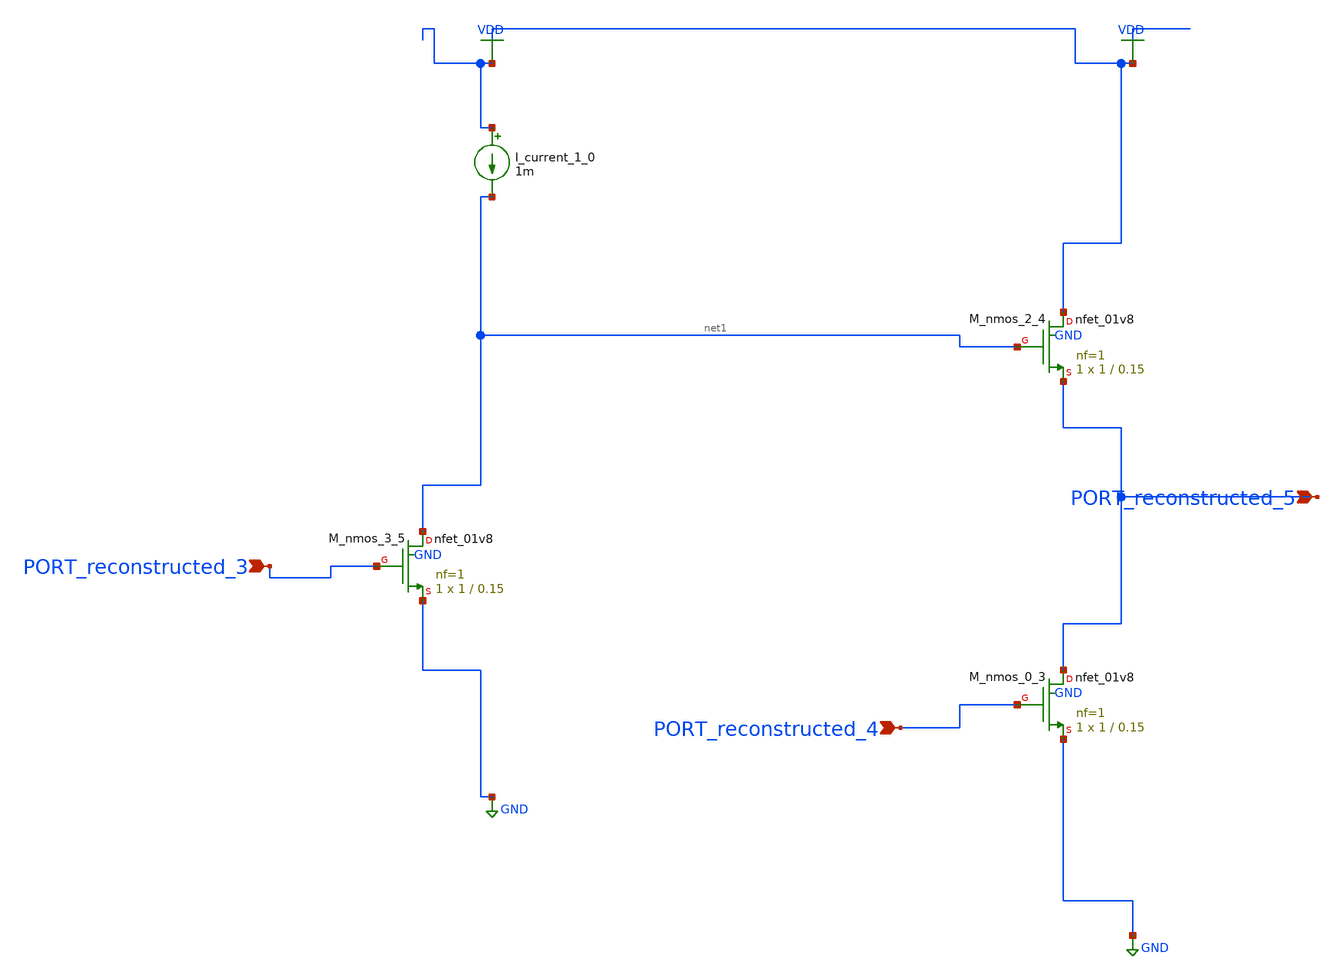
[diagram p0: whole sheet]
** sch_path: schematics/AMSNet/107.sch
**.subckt 107 PORT_reconstructed_4 PORT_reconstructed_3 PORT_reconstructed_5
*.ipin PORT_reconstructed_4
*.ipin PORT_reconstructed_3
*.ipin PORT_reconstructed_5
I_current_1_0 VDD net1 1m
XM_nmos_0_3 PORT_reconstructed_5 PORT_reconstructed_4 GND GND sky130_fd_pr__nfet_01v8 L=0.15 W=1 nf=1
+ ad='int((1 + 1)/2) * 1 / 1 * 0.29' as='int((1 + 2)/2) * 1 / 1 * 0.29' pd='2*int((1 + 1)/2) * (1 / 1 + 0.29)'
+ ps='2*int((1 + 2)/2) * (1 / 1 + 0.29)' nrd='0.29 / 1 ' nrs='0.29 / 1 ' sa=0 sb=0 sd=0 mult=1 m=1
XM_nmos_2_4 VDD net1 PORT_reconstructed_5 GND sky130_fd_pr__nfet_01v8 L=0.15 W=1 nf=1 ad='int((1 + 1)/2) * 1 / 1 * 0.29'
+ as='int((1 + 2)/2) * 1 / 1 * 0.29' pd='2*int((1 + 1)/2) * (1 / 1 + 0.29)' ps='2*int((1 + 2)/2) * (1 / 1 + 0.29)'
+ nrd='0.29 / 1 ' nrs='0.29 / 1 ' sa=0 sb=0 sd=0 mult=1 m=1
XM_nmos_3_5 net1 PORT_reconstructed_3 GND GND sky130_fd_pr__nfet_01v8 L=0.15 W=1 nf=1 ad='int((1 + 1)/2) * 1 / 1 * 0.29'
+ as='int((1 + 2)/2) * 1 / 1 * 0.29' pd='2*int((1 + 1)/2) * (1 / 1 + 0.29)' ps='2*int((1 + 2)/2) * (1 / 1 + 0.29)'
+ nrd='0.29 / 1 ' nrs='0.29 / 1 ' sa=0 sb=0 sd=0 mult=1 m=1
**.ends
.GLOBAL GND
.GLOBAL VDD
.end
